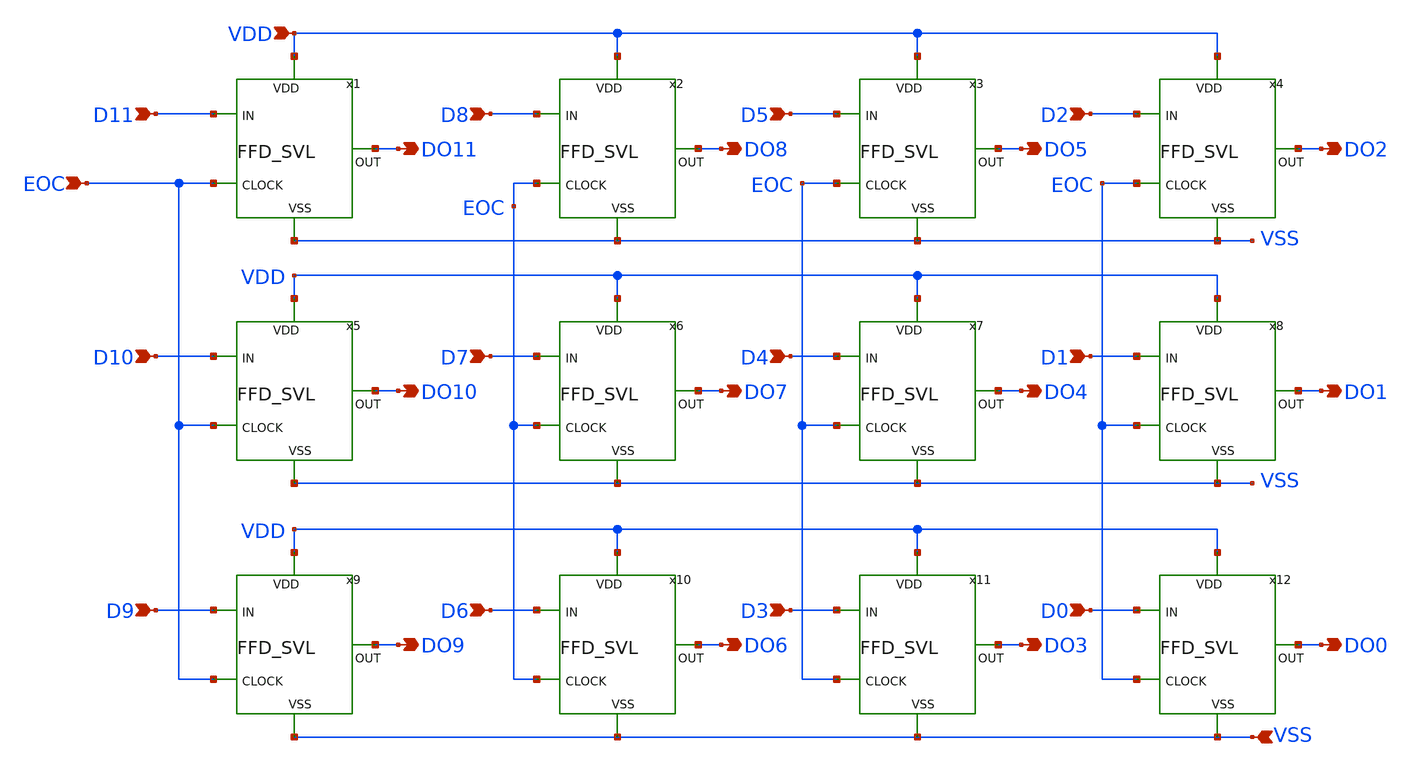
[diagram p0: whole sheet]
** sch_path: SAR_Register.sch
**.subckt SAR_Register VDD VSS D11 D10 D9 D8 D7 D6 D5 D4 D3 D2 D1 D0 DO11 DO10 DO9 DO8 DO7 DO6 DO3
*+ DO4 DO5 DO2 DO1 DO0 EOC
*.ipin VDD
*.ipin VSS
*.ipin D11
*.ipin D10
*.ipin D9
*.ipin D8
*.ipin D7
*.ipin D6
*.ipin D5
*.ipin D4
*.ipin D3
*.ipin D2
*.ipin D1
*.ipin D0
*.opin DO11
*.opin DO10
*.opin DO9
*.opin DO8
*.opin DO7
*.opin DO6
*.opin DO3
*.opin DO4
*.opin DO5
*.opin DO2
*.opin DO1
*.opin DO0
*.ipin EOC
x1 VDD EOC D11 DO11 VSS FFD_SVL
x2 VDD EOC D8 DO8 VSS FFD_SVL
x3 VDD EOC D5 DO5 VSS FFD_SVL
x4 VDD EOC D2 DO2 VSS FFD_SVL
x5 VDD EOC D10 DO10 VSS FFD_SVL
x6 VDD EOC D7 DO7 VSS FFD_SVL
x7 VDD EOC D4 DO4 VSS FFD_SVL
x8 VDD EOC D1 DO1 VSS FFD_SVL
x9 VDD EOC D9 DO9 VSS FFD_SVL
x10 VDD EOC D6 DO6 VSS FFD_SVL
x11 VDD EOC D3 DO3 VSS FFD_SVL
x12 VDD EOC D0 DO0 VSS FFD_SVL
**.ends

* expanding   symbol:  project/FFD_SVL.sym # of pins=5
** sym_path: FFD_SVL.sym
** sch_path: FFD_SVL.sch
.subckt FFD_SVL VDD CLOCK IN OUT VSS
*.ipin VDD
*.ipin VSS
*.opin OUT
*.ipin IN
*.ipin CLOCK
XM1 net1 CLKB VDD VDD sky130_fd_pr__pfet_01v8 L=0.15 W=1 nf=1 ad='int((nf+1)/2) * W/nf * 0.29' as='int((nf+2)/2) * W/nf * 0.29'
+ pd='2*int((nf+1)/2) * (W/nf + 0.29)' ps='2*int((nf+2)/2) * (W/nf + 0.29)' nrd='0.29 / W' nrs='0.29 / W'
+ sa=0 sb=0 sd=0 mult=1 m=1
XM2 VDD VDD net1 VDD sky130_fd_pr__nfet_01v8 L=0.15 W=1 nf=1 ad='int((nf+1)/2) * W/nf * 0.29' as='int((nf+2)/2) * W/nf * 0.29'
+ pd='2*int((nf+1)/2) * (W/nf + 0.29)' ps='2*int((nf+2)/2) * (W/nf + 0.29)' nrd='0.29 / W' nrs='0.29 / W'
+ sa=0 sb=0 sd=0 mult=1 m=1
XM3 VSS VSS net4 VDD sky130_fd_pr__pfet_01v8 L=0.15 W=1 nf=1 ad='int((nf+1)/2) * W/nf * 0.29' as='int((nf+2)/2) * W/nf * 0.29'
+ pd='2*int((nf+1)/2) * (W/nf + 0.29)' ps='2*int((nf+2)/2) * (W/nf + 0.29)' nrd='0.29 / W' nrs='0.29 / W'
+ sa=0 sb=0 sd=0 mult=1 m=1
XM4 net4 CLK VSS VSS sky130_fd_pr__nfet_01v8 L=0.15 W=1 nf=1 ad='int((nf+1)/2) * W/nf * 0.29' as='int((nf+2)/2) * W/nf * 0.29'
+ pd='2*int((nf+1)/2) * (W/nf + 0.29)' ps='2*int((nf+2)/2) * (W/nf + 0.29)' nrd='0.29 / W' nrs='0.29 / W'
+ sa=0 sb=0 sd=0 mult=1 m=1
XM5 net2 IN net1 VDD sky130_fd_pr__pfet_01v8 L=0.15 W=1 nf=1 ad='int((nf+1)/2) * W/nf * 0.29' as='int((nf+2)/2) * W/nf * 0.29'
+ pd='2*int((nf+1)/2) * (W/nf + 0.29)' ps='2*int((nf+2)/2) * (W/nf + 0.29)' nrd='0.29 / W' nrs='0.29 / W'
+ sa=0 sb=0 sd=0 mult=1 m=1
XM6 OUT net2 net1 VDD sky130_fd_pr__pfet_01v8 L=0.15 W=1 nf=1 ad='int((nf+1)/2) * W/nf * 0.29' as='int((nf+2)/2) * W/nf * 0.29'
+ pd='2*int((nf+1)/2) * (W/nf + 0.29)' ps='2*int((nf+2)/2) * (W/nf + 0.29)' nrd='0.29 / W' nrs='0.29 / W'
+ sa=0 sb=0 sd=0 mult=1 m=1
XM7 net2 CLK net3 VSS sky130_fd_pr__nfet_01v8 L=0.15 W=1 nf=1 ad='int((nf+1)/2) * W/nf * 0.29' as='int((nf+2)/2) * W/nf * 0.29'
+ pd='2*int((nf+1)/2) * (W/nf + 0.29)' ps='2*int((nf+2)/2) * (W/nf + 0.29)' nrd='0.29 / W' nrs='0.29 / W'
+ sa=0 sb=0 sd=0 mult=1 m=1
XM8 net3 IN net4 VSS sky130_fd_pr__nfet_01v8 L=0.15 W=1 nf=1 ad='int((nf+1)/2) * W/nf * 0.29' as='int((nf+2)/2) * W/nf * 0.29'
+ pd='2*int((nf+1)/2) * (W/nf + 0.29)' ps='2*int((nf+2)/2) * (W/nf + 0.29)' nrd='0.29 / W' nrs='0.29 / W'
+ sa=0 sb=0 sd=0 mult=1 m=1
XM9 OUT net3 net4 VSS sky130_fd_pr__nfet_01v8 L=0.15 W=1 nf=1 ad='int((nf+1)/2) * W/nf * 0.29' as='int((nf+2)/2) * W/nf * 0.29'
+ pd='2*int((nf+1)/2) * (W/nf + 0.29)' ps='2*int((nf+2)/2) * (W/nf + 0.29)' nrd='0.29 / W' nrs='0.29 / W'
+ sa=0 sb=0 sd=0 mult=1 m=1
x7 VDD CLOCK CLKB VSS Inverter
x8 VDD CLKB CLK VSS Inverter
.ends


* expanding   symbol:  project/Inverter.sym # of pins=4
** sym_path: Inverter.sym
** sch_path: Inverter.sch
.subckt Inverter VDD IN OUT VSS
*.ipin IN
*.ipin VSS
*.ipin VDD
*.opin OUT
XM1 OUT IN VSS VSS sky130_fd_pr__nfet_01v8 L=0.3 W=1 nf=1 ad='int((nf+1)/2) * W/nf * 0.29' as='int((nf+2)/2) * W/nf * 0.29'
+ pd='2*int((nf+1)/2) * (W/nf + 0.29)' ps='2*int((nf+2)/2) * (W/nf + 0.29)' nrd='0.29 / W' nrs='0.29 / W'
+ sa=0 sb=0 sd=0 mult=1 m=1
XM2 OUT IN VDD VDD sky130_fd_pr__pfet_01v8 L=0.3 W=2 nf=1 ad='int((nf+1)/2) * W/nf * 0.29' as='int((nf+2)/2) * W/nf * 0.29'
+ pd='2*int((nf+1)/2) * (W/nf + 0.29)' ps='2*int((nf+2)/2) * (W/nf + 0.29)' nrd='0.29 / W' nrs='0.29 / W'
+ sa=0 sb=0 sd=0 mult=1 m=1
.ends

.end
